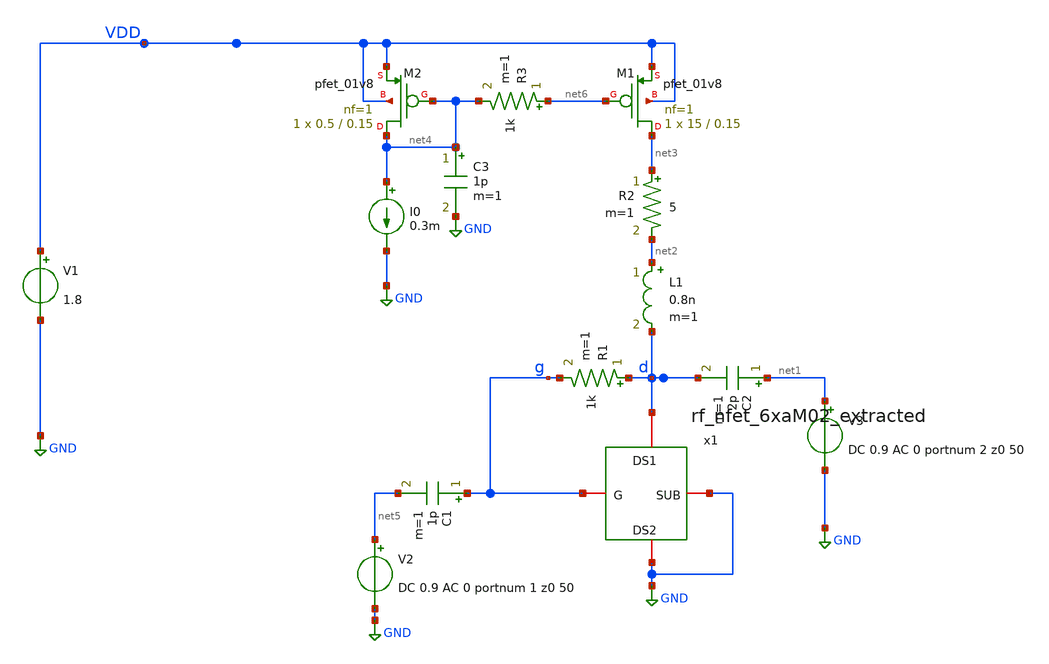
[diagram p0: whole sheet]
** sch_path: xschem/dumb_amp_r1_2.sch
**.subckt dumb_amp_r1_2
V1 VDD GND 1.8
V3 net1 GND DC 0.9 AC 0 portnum 2 z0 50
V2 net5 GND DC 0.9 AC 0 portnum 1 z0 50
C1 g net5 1p m=1
C2 net1 d 2p m=1
x1 g d GND GND rf_nfet_6xaM02_extracted
L1 net2 d 0.8n m=1
R1 d g 1k m=1
R2 net3 net2 5 m=1
XM1 net3 net6 VDD VDD sky130_fd_pr__pfet_01v8 L=0.15 W=15 nf=1 ad='int((nf+1)/2) * W/nf * 0.29' as='int((nf+2)/2) * W/nf * 0.29'
+ pd='2*int((nf+1)/2) * (W/nf + 0.29)' ps='2*int((nf+2)/2) * (W/nf + 0.29)' nrd='0.29 / W' nrs='0.29 / W'
+ sa=0 sb=0 sd=0 mult=1 m=1
XM2 net4 net4 VDD VDD sky130_fd_pr__pfet_01v8 L=0.15 W=0.5 nf=1 ad='int((nf+1)/2) * W/nf * 0.29' as='int((nf+2)/2) * W/nf * 0.29'
+ pd='2*int((nf+1)/2) * (W/nf + 0.29)' ps='2*int((nf+2)/2) * (W/nf + 0.29)' nrd='0.29 / W' nrs='0.29 / W'
+ sa=0 sb=0 sd=0 mult=1 m=1
I0 net4 GND 0.3m
C3 net4 GND 1p m=1
R3 net6 net4 1k m=1
**** begin user architecture code
.lib $::SKYWATER_MODELS/sky130.lib.spice tt
* .include $::PDKPATH/libs.ref/sky130_fd_sc_hvl/spice/sky130_fd_sc_hvl.spice


.subckt DUT_PEX A Y VHI VLO
R0 A Y sky130_fd_pr__res_generic_po w=460000u l=6.54e+06u
X0 Y A VHI VHI sky130_fd_pr__pfet_01v8 ad=0p pd=0u as=0p ps=0u w=4e+06u l=150000u
X1 VHI A Y VHI sky130_fd_pr__pfet_01v8 ad=0p pd=0u as=0p ps=0u w=4e+06u l=150000u
X2 Y A VHI VHI sky130_fd_pr__pfet_01v8 ad=0p pd=0u as=0p ps=0u w=4e+06u l=150000u
X3 Y A VHI VHI sky130_fd_pr__pfet_01v8 ad=0p pd=0u as=0p ps=0u w=4e+06u l=150000u
X4 Y A VHI VHI sky130_fd_pr__pfet_01v8 ad=0p pd=0u as=0p ps=0u w=4e+06u l=150000u
X5 VHI A Y VHI sky130_fd_pr__pfet_01v8 ad=0p pd=0u as=0p ps=0u w=4e+06u l=150000u
X6 VHI A Y VHI sky130_fd_pr__pfet_01v8 ad=0p pd=0u as=0p ps=0u w=4e+06u l=150000u
X7 VHI A Y VHI sky130_fd_pr__pfet_01v8 ad=0p pd=0u as=0p ps=0u w=4e+06u l=150000u
X8 VHI A Y VHI sky130_fd_pr__pfet_01v8 ad=0p pd=0u as=0p ps=0u w=4e+06u l=150000u
X9 Y A VHI VHI sky130_fd_pr__pfet_01v8 ad=0p pd=0u as=0p ps=0u w=4e+06u l=150000u
X10 VHI A Y VHI sky130_fd_pr__pfet_01v8 ad=0p pd=0u as=0p ps=0u w=4e+06u l=150000u
X11 Y A VHI VHI sky130_fd_pr__pfet_01v8 ad=0p pd=0u as=0p ps=0u w=4e+06u l=150000u
X12 VHI A Y VHI sky130_fd_pr__pfet_01v8 ad=0p pd=0u as=0p ps=0u w=4e+06u l=150000u
X13 Y A VHI VHI sky130_fd_pr__pfet_01v8 ad=0p pd=0u as=0p ps=0u w=4e+06u l=150000u
X14 Y A VHI VHI sky130_fd_pr__pfet_01v8 ad=0p pd=0u as=0p ps=0u w=4e+06u l=150000u
X15 Y A VHI VHI sky130_fd_pr__pfet_01v8 ad=0p pd=0u as=0p ps=0u w=4e+06u l=150000u
X16 VHI A Y VHI sky130_fd_pr__pfet_01v8 ad=0p pd=0u as=0p ps=0u w=4e+06u l=150000u
X17 VHI A Y VHI sky130_fd_pr__pfet_01v8 ad=0p pd=0u as=0p ps=0u w=4e+06u l=150000u
X18 VHI A Y VHI sky130_fd_pr__pfet_01v8 ad=0p pd=0u as=0p ps=0u w=4e+06u l=150000u
X19 Y A VHI VHI sky130_fd_pr__pfet_01v8 ad=0p pd=0u as=0p ps=0u w=4e+06u l=150000u
X20 Y A VHI VHI sky130_fd_pr__pfet_01v8 ad=0p pd=0u as=0p ps=0u w=4e+06u l=150000u
X21 VHI A Y VHI sky130_fd_pr__pfet_01v8 ad=0p pd=0u as=0p ps=0u w=4e+06u l=150000u
X22 VHI A Y VHI sky130_fd_pr__pfet_01v8 ad=0p pd=0u as=0p ps=0u w=4e+06u l=150000u
X23 VHI A Y VHI sky130_fd_pr__pfet_01v8 ad=0p pd=0u as=0p ps=0u w=4e+06u l=150000u
X24 Y A VHI VHI sky130_fd_pr__pfet_01v8 ad=0p pd=0u as=0p ps=0u w=4e+06u l=150000u
X25 Y A VHI VHI sky130_fd_pr__pfet_01v8 ad=0p pd=0u as=0p ps=0u w=4e+06u l=150000u
X26 Y A VHI VHI sky130_fd_pr__pfet_01v8 ad=0p pd=0u as=0p ps=0u w=4e+06u l=150000u
X27 Y A VHI VHI sky130_fd_pr__pfet_01v8 ad=0p pd=0u as=0p ps=0u w=4e+06u l=150000u
X28 Y A VHI VHI sky130_fd_pr__pfet_01v8 ad=0p pd=0u as=0p ps=0u w=4e+06u l=150000u
X29 VHI A Y VHI sky130_fd_pr__pfet_01v8 ad=0p pd=0u as=0p ps=0u w=4e+06u l=150000u
X30 VHI A Y VHI sky130_fd_pr__pfet_01v8 ad=0p pd=0u as=0p ps=0u w=4e+06u l=150000u
X31 VHI A Y VHI sky130_fd_pr__pfet_01v8 ad=0p pd=0u as=0p ps=0u w=4e+06u l=150000u
X32 VLO A Y VLO sky130_fd_pr__nfet_01v8 ad=0p pd=0u as=0p ps=0u w=4e+06u l=150000u
X33 Y A VLO VLO sky130_fd_pr__nfet_01v8 ad=0p pd=0u as=0p ps=0u w=4e+06u l=150000u
X34 Y A VLO VLO sky130_fd_pr__nfet_01v8 ad=0p pd=0u as=0p ps=0u w=4e+06u l=150000u
X35 Y A VLO VLO sky130_fd_pr__nfet_01v8 ad=0p pd=0u as=0p ps=0u w=4e+06u l=150000u
X36 VLO A Y VLO sky130_fd_pr__nfet_01v8 ad=0p pd=0u as=0p ps=0u w=4e+06u l=150000u
X37 Y A VLO VLO sky130_fd_pr__nfet_01v8 ad=0p pd=0u as=0p ps=0u w=4e+06u l=150000u
X38 VLO A Y VLO sky130_fd_pr__nfet_01v8 ad=0p pd=0u as=0p ps=0u w=4e+06u l=150000u
X39 Y A VLO VLO sky130_fd_pr__nfet_01v8 ad=0p pd=0u as=0p ps=0u w=4e+06u l=150000u
X40 Y A VLO VLO sky130_fd_pr__nfet_01v8 ad=0p pd=0u as=0p ps=0u w=4e+06u l=150000u
X41 VLO A Y VLO sky130_fd_pr__nfet_01v8 ad=0p pd=0u as=0p ps=0u w=4e+06u l=150000u
X42 VLO A Y VLO sky130_fd_pr__nfet_01v8 ad=0p pd=0u as=0p ps=0u w=4e+06u l=150000u
X43 VLO A Y VLO sky130_fd_pr__nfet_01v8 ad=0p pd=0u as=0p ps=0u w=4e+06u l=150000u
X44 Y A VLO VLO sky130_fd_pr__nfet_01v8 ad=0p pd=0u as=0p ps=0u w=4e+06u l=150000u
X45 Y A VLO VLO sky130_fd_pr__nfet_01v8 ad=0p pd=0u as=0p ps=0u w=4e+06u l=150000u
X46 VLO A Y VLO sky130_fd_pr__nfet_01v8 ad=0p pd=0u as=0p ps=0u w=4e+06u l=150000u
X47 VLO A Y VLO sky130_fd_pr__nfet_01v8 ad=0p pd=0u as=0p ps=0u w=4e+06u l=150000u
C0 VLO Y 37.95fF
C1 VLO VHI 5.31fF
C2 VLO A 10.01fF
C3 Y VHI 74.69fF
C4 A Y 21.97fF
C5 A VHI 23.59fF
C6 VLO 0 8.21fF
C7 Y 0 2.50fF
C8 A 0 2.76fF
C9 VHI 0 14.48fF
.ends

XDUT A Y VDD GND DUT_PEX

.sp dec 1000 1e9 10e9 1


* .ac dec 1000 0.01e9 100e9
.control
run
display

let z11=50*(1+s_1_1)/(1-s_1_1)
let z22=50*(1+s_2_2)/(1-s_2_2)
let S11 = S_1_1
let S21 = S_2_1
let S12 = S_1_2
let S22 = S_2_2

* Stability
let delta=S11*S22-S12*S21
let K    = (1-mag(S11)^2-mag(S22)^2+mag(delta)^2)/(2*mag(S12*S21))
let mu   = (1-mag(S11)^2)/(mag(S22-conj(S11)*delta)+mag(S21*S12))
* plot real(z11) real(z22)
* plot imag(z11) imag(z22)
plot db(S_1_1) db(S_2_2) db(S_2_1)
*
plot db(K)
plot mag(delta)
plot db(mu)
plot NF NFmin
.endc


**** end user architecture code
**.ends

* expanding   symbol:  rf_nfet_6xaM02_extracted.sym # of pins=4
** sym_path: xschem/rf_nfet_6xaM02_extracted.sym
** sch_path: xschem/rf_nfet_6xaM02_extracted.sch
.subckt rf_nfet_6xaM02_extracted G DS1 DS2 SUB
*.iopin G
*.iopin DS1
*.iopin DS2
*.iopin SUB
**** begin user architecture code


* Extraction of 6xaM02 (12 finger) Transistors
* wt=60um, L=0.15um
.subckt NFET_extract_1 SD1 G2 SD2 SUB

* .subckt sky130_fd_pr__rf_nfet_01v8_aM02W5p00L0p15 DRAIN GATE SOURCE SUBSTRATE
*  X0 DRAIN GATE SOURCE SUBSTRATE sky130_fd_pr__nfet_01v8 ad=1.414e+12p pd=1.066e+07u as=2.828e+12p
*+ ps=2.132e+07u w=5.05e+06u l=150000u
*  X1 SOURCE GATE DRAIN SUBSTRATE sky130_fd_pr__nfet_01v8 ad=0p pd=0u as=0p ps=0u w=5.05e+06u
*+ l=150000u
*  C0 SOURCE DRAIN 3.73fF
*  C1 SOURCE SUBSTRATE 2.58fF
* .ends

X0 SD1 G2 SD2 SUB sky130_fd_pr__nfet_01v8 ad=0p pd=0u as=0p ps=0u w=5.05e+06u l=150000u
X1 SD1 G2 SD2 SUB sky130_fd_pr__nfet_01v8 ad=0p pd=0u as=0p ps=0u w=5.05e+06u l=150000u
X2 SD2 G2 SD1 SUB sky130_fd_pr__nfet_01v8 ad=0p pd=0u as=0p ps=0u w=5.05e+06u l=150000u
X3 SD2 G2 SD1 SUB sky130_fd_pr__nfet_01v8 ad=0p pd=0u as=0p ps=0u w=5.05e+06u l=150000u
X4 SD1 G2 SD2 SUB sky130_fd_pr__nfet_01v8 ad=0p pd=0u as=0p ps=0u w=5.05e+06u l=150000u
X5 SD1 G2 SD2 SUB sky130_fd_pr__nfet_01v8 ad=0p pd=0u as=0p ps=0u w=5.05e+06u l=150000u
X6 SD2 G2 SD1 SUB sky130_fd_pr__nfet_01v8 ad=0p pd=0u as=0p ps=0u w=5.05e+06u l=150000u
X7 SD2 G2 SD1 SUB sky130_fd_pr__nfet_01v8 ad=0p pd=0u as=0p ps=0u w=5.05e+06u l=150000u
X8 SD1 G2 SD2 SUB sky130_fd_pr__nfet_01v8 ad=0p pd=0u as=0p ps=0u w=5.05e+06u l=150000u
X9 SD1 G2 SD2 SUB sky130_fd_pr__nfet_01v8 ad=0p pd=0u as=0p ps=0u w=5.05e+06u l=150000u
X10 SD2 G2 SD1 SUB sky130_fd_pr__nfet_01v8 ad=0p pd=0u as=0p ps=0u w=5.05e+06u l=150000u
X11 SD2 G2 SD1 SUB sky130_fd_pr__nfet_01v8 ad=0p pd=0u as=0p ps=0u w=5.05e+06u l=150000u
C0 SD2 G2 3.50fF
C1 SUB SD1 3.01fF
C2 G2 SD1 4.50fF
C3 G2 SUB 2.28fF
C4 SD2 SD1 30.48fF
C5 G2 SUB 3.11fF
C6 SD1 SUB 6.76fF

* C0 B G 2.85fF
* C1 S D 22.23fF
* C2 G D 5.77fF
* C3 S G 7.53fF
* Xnfet_3x_2_0/sky130_fd_pr__rf_nfet_01v8_aM02W5p00L0p15_0 D G S B
*+ sky130_fd_pr__rf_nfet_01v8_aM02W5p00L0p15
* Xnfet_3x_2_0/sky130_fd_pr__rf_nfet_01v8_aM02W5p00L0p15_1 D G S B
*+ sky130_fd_pr__rf_nfet_01v8_aM02W5p00L0p15
* Xnfet_3x_2_0/sky130_fd_pr__rf_nfet_01v8_aM02W5p00L0p15_2 D G S B
*+ sky130_fd_pr__rf_nfet_01v8_aM02W5p00L0p15
* Xnfet_3x_2_1/sky130_fd_pr__rf_nfet_01v8_aM02W5p00L0p15_0 D G S B
*+ sky130_fd_pr__rf_nfet_01v8_aM02W5p00L0p15
* Xnfet_3x_2_1/sky130_fd_pr__rf_nfet_01v8_aM02W5p00L0p15_1 D G S B
*+ sky130_fd_pr__rf_nfet_01v8_aM02W5p00L0p15
* Xnfet_3x_2_1/sky130_fd_pr__rf_nfet_01v8_aM02W5p00L0p15_2 D G S B
*+ sky130_fd_pr__rf_nfet_01v8_aM02W5p00L0p15
* C4 S B 13.70fF
* C5 G B 3.35fF

.ends

XM0 DS1 G DS2 SUB NFET_extract_1


**** end user architecture code
.ends

.GLOBAL GND
.end
